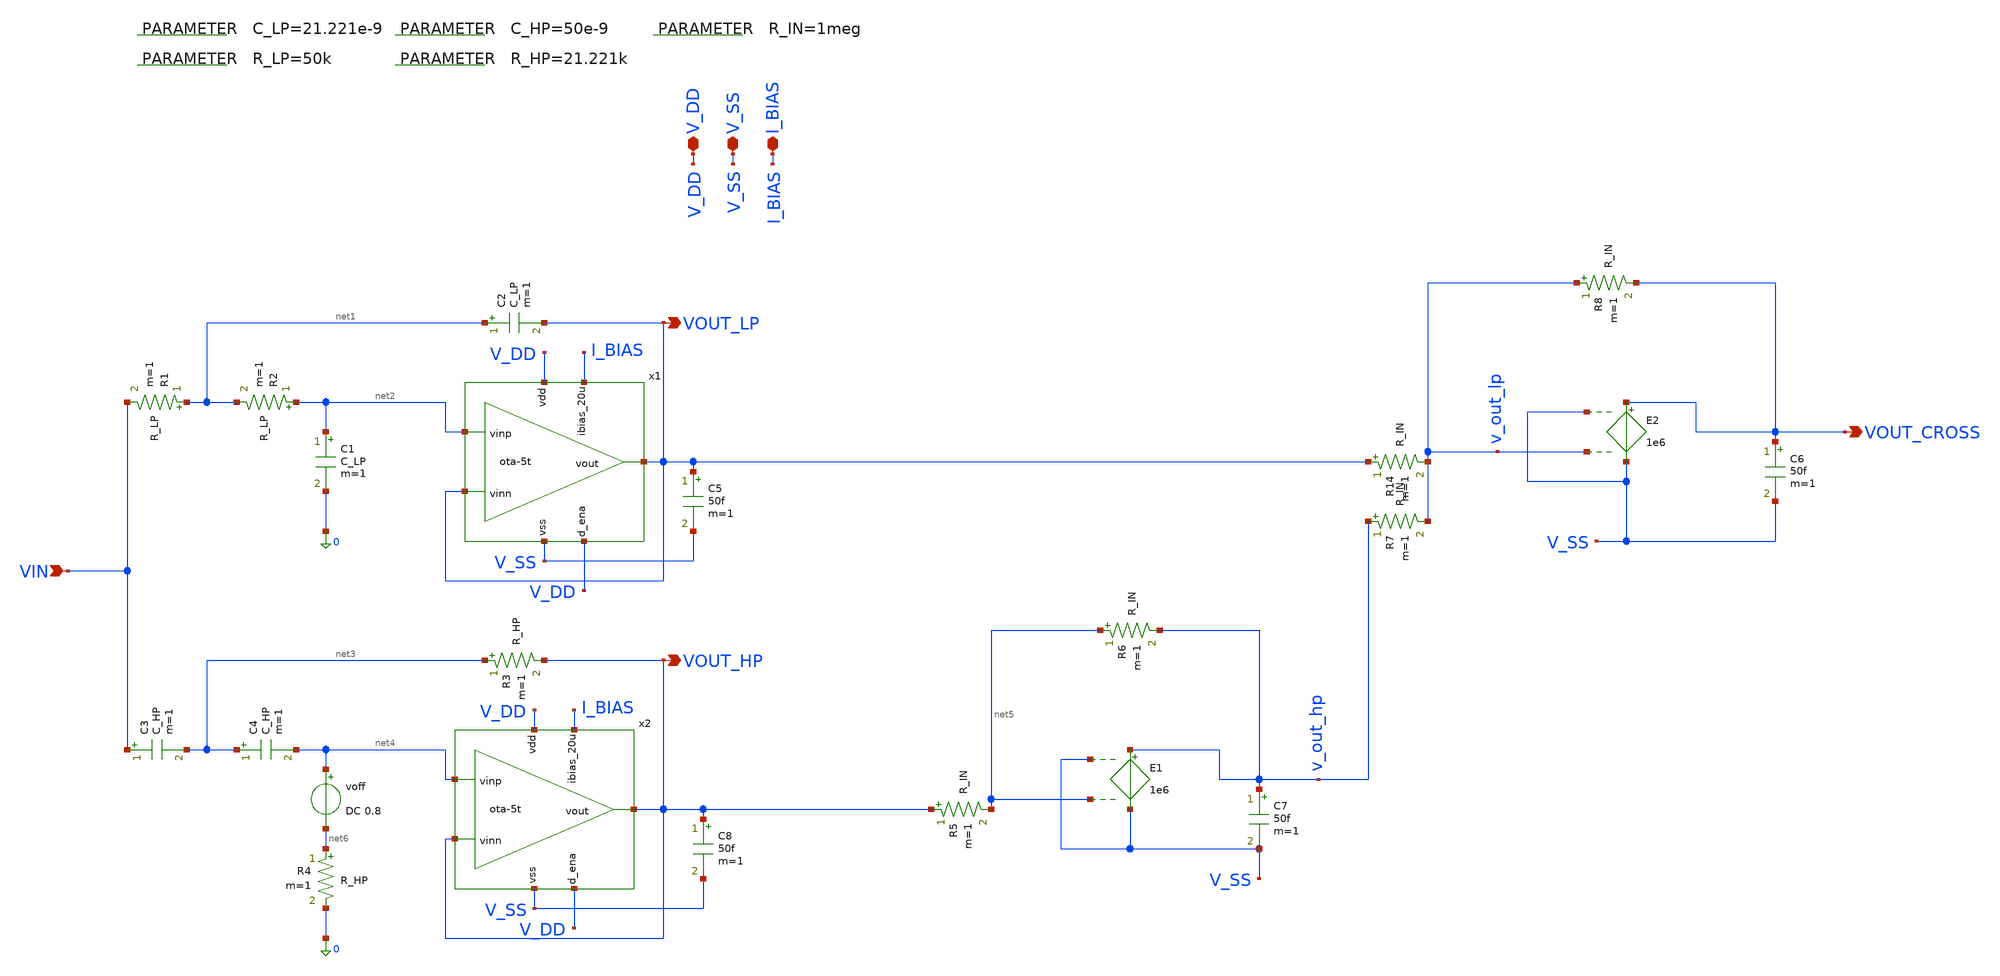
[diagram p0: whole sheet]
** sch_path: 004_Real_Circuits/001_version_basic_ota_pretl/linkwtz_riley_crossover_pretl_OTA.sch
* 004_Real_Circuits/001_version_basic_ota_pretl/ota-5t.sch:
* (c) 2024-2025 Harald Pretl, Apache-2.0 license
**.subckt linkwtz_riley_crossover_pretl_OTA VOUT_LP VIN V_DD VOUT_HP V_SS I_BIAS VOUT_CROSS
*.opin VOUT_LP
*.ipin VIN
*.iopin V_DD
*.opin VOUT_HP
*.iopin V_SS
*.iopin I_BIAS
*.opin VOUT_CROSS
R1 net1 VIN R_LP m=1
.param R_IN=1meg
R2 net2 net1 R_LP m=1
C1 net2 0 C_LP m=1
C2 net1 VOUT_LP C_LP m=1
C3 VIN net3 C_HP m=1
C4 net3 net4 C_HP m=1
R3 net3 VOUT_HP R_HP m=1
R4 net6 0 R_HP m=1
R5 VOUT_HP net5 R_IN m=1
R6 net5 v_out_hp R_IN m=1
R14 VOUT_LP v_out_lp R_IN m=1
R7 v_out_hp v_out_lp R_IN m=1
R8 v_out_lp VOUT_CROSS R_IN m=1
.param C_LP=21.221e-9
.param R_LP=50k
.param C_HP=50e-9
.param R_HP=21.221k
C5 VOUT_LP V_SS 50f m=1
C6 VOUT_CROSS V_SS 50f m=1
C7 v_out_hp V_SS 50f m=1
C8 VOUT_HP V_SS 50f m=1
voff net4 net6 DC 0.8
E1 v_out_hp V_SS V_SS net5 1e6
E2 VOUT_CROSS V_SS V_SS v_out_lp 1e6
x1 V_DD VOUT_LP net2 VOUT_LP I_BIAS V_DD V_SS ota-5t
x2 V_DD VOUT_HP net4 VOUT_HP I_BIAS V_DD V_SS ota-5t
**.ends

* expanding   symbol:  004_Real_Circuits/001_version_basic_ota_pretl/ota-5t.sym # of pins=7
** sym_path: 004_Real_Circuits/001_version_basic_ota_pretl/ota-5t.sym
** sch_path: 004_Real_Circuits/001_version_basic_ota_pretl/ota-5t.sch
.subckt ota-5t vdd vout vinp vinn ibias_20u d_ena vss
*.ipin ibias_20u
*.iopin vdd
*.iopin vss
*.ipin vinp
*.ipin vinn
*.opin vout
*.ipin d_ena
XM5 tail gate_n vss vss sg13_lv_nmos w=1.5u l=5u ng=1 m=1 mm_ok=1
XM4 vout gate_p vdd vdd sg13_lv_pmos w=3.5u l=5u ng=1 m=1 mm_ok=1
XM1 gate_p vinp tail vss sg13_lv_nmos w=2u l=5u ng=1 m=1 mm_ok=1
XM2 vout vinn tail vss sg13_lv_nmos w=2u l=5u ng=1 m=1 mm_ok=1
XM3 gate_p gate_p vdd vdd sg13_lv_pmos w=3.5u l=5u ng=1 m=1 mm_ok=1
XM6 ibias_20u gate_n vss vss sg13_lv_nmos w=10u l=5u ng=5 m=1 mm_ok=1
XM9 gate_n ena_n vss vss sg13_lv_nmos w=0.5u l=0.13u ng=1 m=1 mm_ok=1
XM11 gate_p ena vdd vdd sg13_lv_pmos w=1.5u l=0.13u ng=1 m=1 mm_ok=1
XM7 ena ena_n vss vss sg13_lv_nmos w=0.5u l=0.13u ng=1 m=1 mm_ok=1
XM8 ena ena_n vdd vdd sg13_lv_pmos w=1.5u l=0.13u ng=1 m=1 mm_ok=1
XM10 ibias_20u ena gate_n vss sg13_lv_nmos w=0.5u l=0.13u ng=1 m=1 mm_ok=1
XM12 ena_n d_ena vss vss sg13_lv_nmos w=0.5u l=0.13u ng=1 m=1 mm_ok=1
XM13 ena_n d_ena vdd vdd sg13_lv_pmos w=1.5u l=0.13u ng=1 m=1 mm_ok=1
.ends

.end
